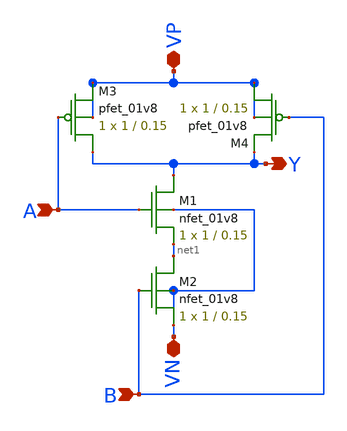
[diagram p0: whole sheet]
** sch_path: miniproject_01/xschem/nand2.sch
**.subckt nand2 Y B A VP VN
*.opin Y
*.ipin B
*.ipin A
*.iopin VP
*.iopin VN
XM1 Y A net1 VN sky130_fd_pr__nfet_01v8 L=0.15 W=1 nf=1 ad='int((nf+1)/2) * W/nf * 0.29' as='int((nf+2)/2) * W/nf * 0.29'
+ pd='2*int((nf+1)/2) * (W/nf + 0.29)' ps='2*int((nf+2)/2) * (W/nf + 0.29)' nrd='0.29 / W' nrs='0.29 / W'
+ sa=0 sb=0 sd=0 mult=1 m=1
XM2 net1 B VN VN sky130_fd_pr__nfet_01v8 L=0.15 W=1 nf=1 ad='int((nf+1)/2) * W/nf * 0.29' as='int((nf+2)/2) * W/nf * 0.29'
+ pd='2*int((nf+1)/2) * (W/nf + 0.29)' ps='2*int((nf+2)/2) * (W/nf + 0.29)' nrd='0.29 / W' nrs='0.29 / W'
+ sa=0 sb=0 sd=0 mult=1 m=1
XM3 Y A VP VP sky130_fd_pr__pfet_01v8 L=0.15 W=1 nf=1 ad='int((nf+1)/2) * W/nf * 0.29' as='int((nf+2)/2) * W/nf * 0.29'
+ pd='2*int((nf+1)/2) * (W/nf + 0.29)' ps='2*int((nf+2)/2) * (W/nf + 0.29)' nrd='0.29 / W' nrs='0.29 / W'
+ sa=0 sb=0 sd=0 mult=1 m=1
XM4 VP B Y VP sky130_fd_pr__pfet_01v8 L=0.15 W=1 nf=1 ad='int((nf+1)/2) * W/nf * 0.29' as='int((nf+2)/2) * W/nf * 0.29'
+ pd='2*int((nf+1)/2) * (W/nf + 0.29)' ps='2*int((nf+2)/2) * (W/nf + 0.29)' nrd='0.29 / W' nrs='0.29 / W'
+ sa=0 sb=0 sd=0 mult=1 m=1
**.ends
.end
